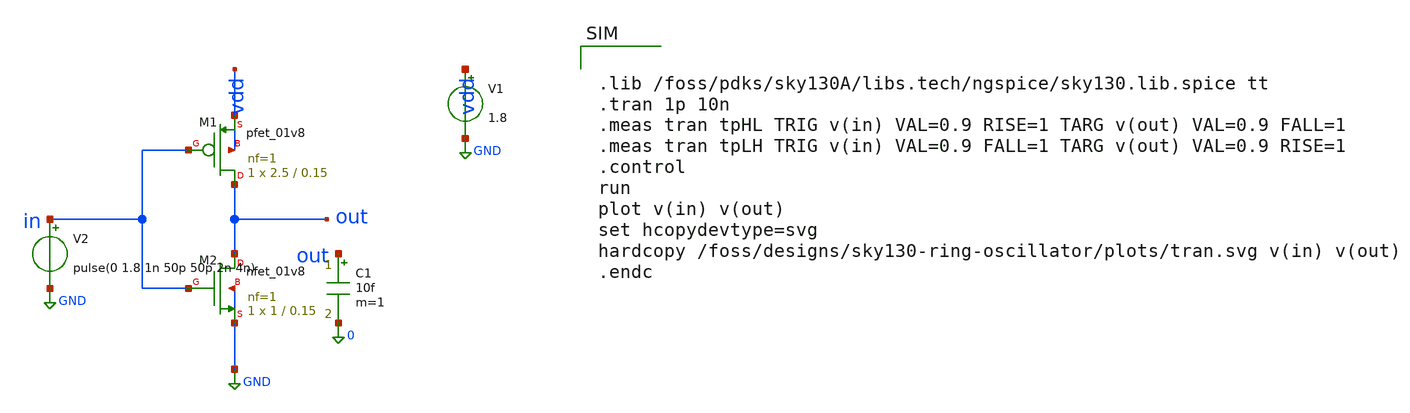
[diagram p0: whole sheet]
** sch_path: xschem/inverter_tran.sch
**.subckt inverter_tran
XM1 out in vdd vdd sky130_fd_pr__pfet_01v8 L=0.15 W=2.5 nf=1 ad='int((1 + 1)/2) * 2.5 / 1 * 0.29' as='int((1 + 2)/2) * 2.5 / 1 * 0.29'
+ pd='2*int((1 + 1)/2) * (2.5 / 1 + 0.29)' ps='2*int((1 + 2)/2) * (2.5 / 1 + 0.29)' nrd='0.29 / 2.5 ' nrs='0.29 / 2.5 '
+ sa=0 sb=0 sd=0 mult=1 m=1
XM2 out in GND GND sky130_fd_pr__nfet_01v8 L=0.15 W=1 nf=1 ad='int((1 + 1)/2) * 1 / 1 * 0.29' as='int((1 + 2)/2) * 1 / 1 * 0.29'
+ pd='2*int((1 + 1)/2) * (1 / 1 + 0.29)' ps='2*int((1 + 2)/2) * (1 / 1 + 0.29)' nrd='0.29 / 1 ' nrs='0.29 / 1 '
+ sa=0 sb=0 sd=0 mult=1 m=1
V1 vdd GND 1.8
V2 in GND pulse(0 1.8 1n 50p 50p 2n 4n)
C1 out 0 10f m=1
**** begin user architecture code


.lib /foss/pdks/sky130A/libs.tech/ngspice/sky130.lib.spice tt
.tran 1p 10n
.meas tran tpHL TRIG v(in) VAL=0.9 RISE=1 TARG v(out) VAL=0.9 FALL=1
.meas tran tpLH TRIG v(in) VAL=0.9 FALL=1 TARG v(out) VAL=0.9 RISE=1
.control
run
plot v(in) v(out)
set hcopydevtype=svg
hardcopy /foss/designs/sky130-ring-oscillator/plots/tran.svg v(in) v(out)
.endc


**** end user architecture code
**.ends
.GLOBAL GND
.end
